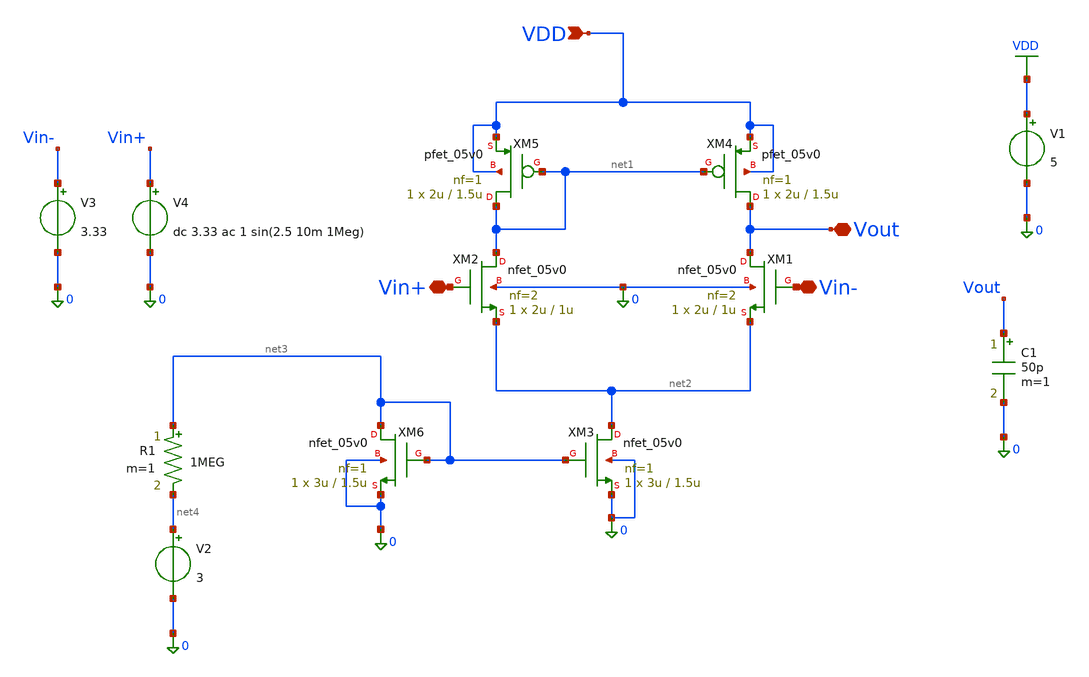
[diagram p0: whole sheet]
** sch_path: TG_gm_ff_testing/gm_ff_testing.sch
**.subckt gm_ff_testing VDD Vin- Vin+ Vout
*.ipin VDD
*.iopin Vin-
*.iopin Vin+
*.iopin Vout
XM1 Vout Vin- net2 0 nfet_05v0 L=1u W=2u nf=2 ad='int((nf+1)/2) * W/nf * 0.18u' as='int((nf+2)/2) * W/nf * 0.18u'
+ pd='2*int((nf+1)/2) * (W/nf + 0.18u)' ps='2*int((nf+2)/2) * (W/nf + 0.18u)' nrd='0.18u / W' nrs='0.18u / W'
+ sa=0 sb=0 sd=0 m=1
XM2 net1 Vin+ net2 0 nfet_05v0 L=1u W=2u nf=2 ad='int((nf+1)/2) * W/nf * 0.18u' as='int((nf+2)/2) * W/nf * 0.18u'
+ pd='2*int((nf+1)/2) * (W/nf + 0.18u)' ps='2*int((nf+2)/2) * (W/nf + 0.18u)' nrd='0.18u / W' nrs='0.18u / W'
+ sa=0 sb=0 sd=0 m=1
XM3 net2 net3 0 0 nfet_05v0 L=1.5u W=3u nf=1 ad='int((nf+1)/2) * W/nf * 0.18u' as='int((nf+2)/2) * W/nf * 0.18u'
+ pd='2*int((nf+1)/2) * (W/nf + 0.18u)' ps='2*int((nf+2)/2) * (W/nf + 0.18u)' nrd='0.18u / W' nrs='0.18u / W'
+ sa=0 sb=0 sd=0 m=1
XM4 Vout net1 VDD VDD pfet_05v0 L=1.5u W=2u nf=1 ad='int((nf+1)/2) * W/nf * 0.18u' as='int((nf+2)/2) * W/nf * 0.18u'
+ pd='2*int((nf+1)/2) * (W/nf + 0.18u)' ps='2*int((nf+2)/2) * (W/nf + 0.18u)' nrd='0.18u / W' nrs='0.18u / W'
+ sa=0 sb=0 sd=0 m=1
XM5 net1 net1 VDD VDD pfet_05v0 L=1.5u W=2u nf=1 ad='int((nf+1)/2) * W/nf * 0.18u' as='int((nf+2)/2) * W/nf * 0.18u'
+ pd='2*int((nf+1)/2) * (W/nf + 0.18u)' ps='2*int((nf+2)/2) * (W/nf + 0.18u)' nrd='0.18u / W' nrs='0.18u / W'
+ sa=0 sb=0 sd=0 m=1
V1 VDD 0 5
V3 Vin- 0 3.33
V4 Vin+ 0 dc 3.33 ac 1 sin(2.5 10m 1Meg)
XM6 net3 net3 0 0 nfet_05v0 L=1.5u W=3u nf=1 ad='int((nf+1)/2) * W/nf * 0.18u' as='int((nf+2)/2) * W/nf * 0.18u'
+ pd='2*int((nf+1)/2) * (W/nf + 0.18u)' ps='2*int((nf+2)/2) * (W/nf + 0.18u)' nrd='0.18u / W' nrs='0.18u / W'
+ sa=0 sb=0 sd=0 m=1
R1 net3 net4 1MEG m=1
V2 net4 0 3
C1 Vout 0 50p m=1
**** begin user architecture code



.include /foss/pdks/gf180mcuD/libs.tech/ngspice/design.ngspice
.lib /foss/pdks/gf180mcuD/libs.tech/ngspice/sm141064.ngspice typical
.lib /foss/pdks/gf180mcuD/libs.tech/ngspice/sm141064.ngspice res_typical

.control
  save all
  op
  print all
  print @m.xm2.m0[gm]
  print @m.xm2.m0[id]
  *show all
  ac dec 10 1 1G
  meas ac dc_gain MAX vdb(Vout)
  meas ac ugbw WHEN vdb(Vout)=0 FALL=1
  let phase_deg = (180/PI)*vp(Vout)
  plot vdb(Vout)
  plot phase_deg
.endc



**** end user architecture code
**.ends
.GLOBAL VDD
.end
